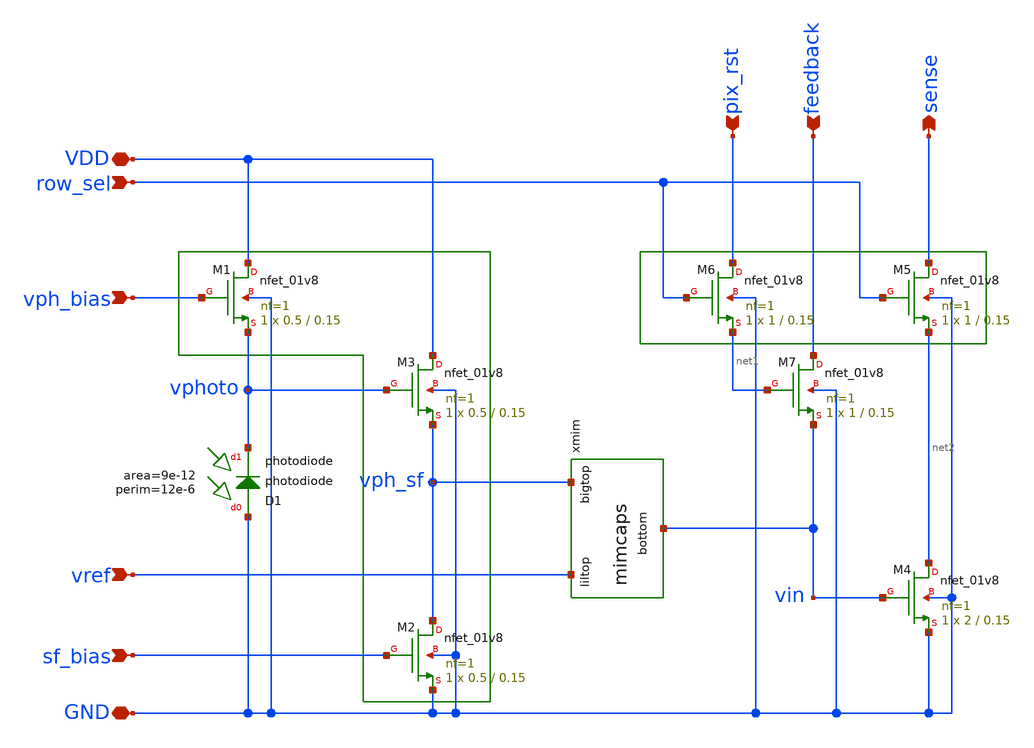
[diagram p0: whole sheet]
** sch_path: analog/xschem/openDVS_pedantic.sch
**.subckt openDVS_pedantic GND VDD row_sel vref vph_bias sf_bias pix_rst feedback sense
*.iopin GND
*.iopin VDD
*.ipin row_sel
*.ipin vref
*.ipin vph_bias
*.ipin sf_bias
*.ipin pix_rst
*.ipin feedback
*.opin sense
XM1 VDD vph_bias vphoto GND sky130_fd_pr__nfet_01v8 L=0.15 W=0.5 nf=1 ad='int((1 + 1)/2) * 0.5 / 1 * 0.29'
+ as='int((1 + 2)/2) * 0.5 / 1 * 0.29' pd='2*int((1 + 1)/2) * (0.5 / 1 + 0.29)' ps='2*int((1 + 2)/2) * (0.5 / 1 + 0.29)'
+ nrd='0.29 / 0.5 ' nrs='0.29 / 0.5 ' sa=0 sb=0 sd=0 mult=1 m=1
XM4 net2 vin GND GND sky130_fd_pr__nfet_01v8 L=0.15 W=2 nf=1 ad='int((1 + 1)/2) * 2 / 1 * 0.29' as='int((1 + 2)/2) * 2 / 1 * 0.29'
+ pd='2*int((1 + 1)/2) * (2 / 1 + 0.29)' ps='2*int((1 + 2)/2) * (2 / 1 + 0.29)' nrd='0.29 / 2 ' nrs='0.29 / 2 '
+ sa=0 sb=0 sd=0 mult=1 m=1
XM7 feedback net1 vin GND sky130_fd_pr__nfet_01v8 L=0.15 W=1 nf=1 ad='int((1 + 1)/2) * 1 / 1 * 0.29'
+ as='int((1 + 2)/2) * 1 / 1 * 0.29' pd='2*int((1 + 1)/2) * (1 / 1 + 0.29)' ps='2*int((1 + 2)/2) * (1 / 1 + 0.29)'
+ nrd='0.29 / 1 ' nrs='0.29 / 1 ' sa=0 sb=0 sd=0 mult=1 m=1
XM2 vph_sf sf_bias GND GND sky130_fd_pr__nfet_01v8 L=0.15 W=0.5 nf=1 ad='int((1 + 1)/2) * 0.5 / 1 * 0.29'
+ as='int((1 + 2)/2) * 0.5 / 1 * 0.29' pd='2*int((1 + 1)/2) * (0.5 / 1 + 0.29)' ps='2*int((1 + 2)/2) * (0.5 / 1 + 0.29)'
+ nrd='0.29 / 0.5 ' nrs='0.29 / 0.5 ' sa=0 sb=0 sd=0 mult=1 m=1
XM3 VDD vphoto vph_sf GND sky130_fd_pr__nfet_01v8 L=0.15 W=0.5 nf=1 ad='int((1 + 1)/2) * 0.5 / 1 * 0.29'
+ as='int((1 + 2)/2) * 0.5 / 1 * 0.29' pd='2*int((1 + 1)/2) * (0.5 / 1 + 0.29)' ps='2*int((1 + 2)/2) * (0.5 / 1 + 0.29)'
+ nrd='0.29 / 0.5 ' nrs='0.29 / 0.5 ' sa=0 sb=0 sd=0 mult=1 m=1
XD1 GND vphoto sky130_fd_pr__photodiode area=9e-12 perim=12e-6
XM5 sense row_sel net2 GND sky130_fd_pr__nfet_01v8 L=0.15 W=1 nf=1 ad='int((1 + 1)/2) * 1 / 1 * 0.29'
+ as='int((1 + 2)/2) * 1 / 1 * 0.29' pd='2*int((1 + 1)/2) * (1 / 1 + 0.29)' ps='2*int((1 + 2)/2) * (1 / 1 + 0.29)'
+ nrd='0.29 / 1 ' nrs='0.29 / 1 ' sa=0 sb=0 sd=0 mult=1 m=1
XM6 pix_rst row_sel net1 GND sky130_fd_pr__nfet_01v8 L=0.15 W=1 nf=1 ad='int((1 + 1)/2) * 1 / 1 * 0.29'
+ as='int((1 + 2)/2) * 1 / 1 * 0.29' pd='2*int((1 + 1)/2) * (1 / 1 + 0.29)' ps='2*int((1 + 2)/2) * (1 / 1 + 0.29)'
+ nrd='0.29 / 1 ' nrs='0.29 / 1 ' sa=0 sb=0 sd=0 mult=1 m=1
xmim vref vph_sf vin mimcaps
**.ends

* expanding   symbol:  mimcaps.sym # of pins=3
** sym_path: analog/xschem/mimcaps.sym
** sch_path: analog/xschem/mimcaps.sch
.subckt mimcaps liltop bigtop bottom
*.iopin bottom
*.iopin liltop
*.iopin bigtop
XCSAMPLE bigtop bottom sky130_fd_pr__cap_mim_m3_1 W=4 L=8 MF=1 m=1
XCREF liltop bottom sky130_fd_pr__cap_mim_m3_1 W=2 L=2 MF=1 m=1
.ends

.end
